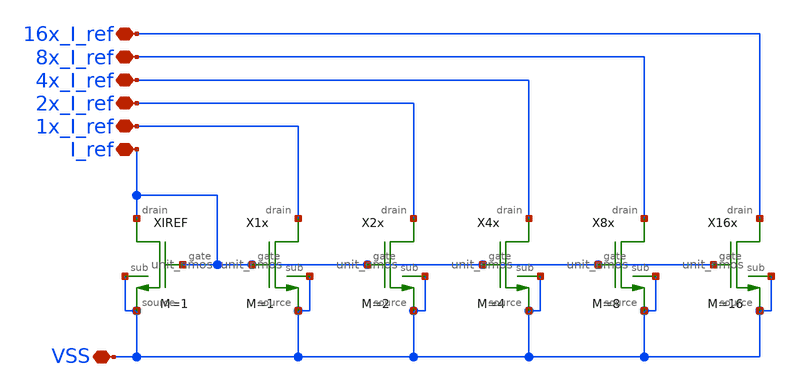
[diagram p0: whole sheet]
** sch_path: designs/libs/core_current_mirror/nmos_current_mirror/nmos_current_mirror.sch
**.subckt nmos_current_mirror I_ref VSS 1x_I_ref 2x_I_ref 4x_I_ref 8x_I_ref 16x_I_ref
*.iopin I_ref
*.iopin VSS
*.iopin 1x_I_ref
*.iopin 2x_I_ref
*.iopin 4x_I_ref
*.iopin 8x_I_ref
*.iopin 16x_I_ref
XIREF I_ref VSS I_ref VSS unit_nmos M=1
X1x 1x_I_ref VSS I_ref VSS unit_nmos M=1
X2x 2x_I_ref VSS I_ref VSS unit_nmos M=2
X4x 4x_I_ref VSS I_ref VSS unit_nmos M=4
X8x 8x_I_ref VSS I_ref VSS unit_nmos M=8
X16x 16x_I_ref VSS I_ref VSS unit_nmos M=16
**.ends

* expanding   symbol:  libs/core_single_mos/unit_nmos/unit_nmos.sym # of pins=4
** sym_path: libs/core_single_mos/unit_nmos/unit_nmos.sym
** sch_path: libs/core_single_mos/unit_nmos/unit_nmos.sch
.subckt unit_nmos drain sub gate source
*.iopin drain
*.iopin source
*.iopin sub
*.iopin gate
XM1 drain gate source sub nfet_03v3 L=0.5u W=12u nf=2 ad='int((nf+1)/2) * W/nf * 0.18u' as='int((nf+2)/2) * W/nf * 0.18u'
+ pd='2*int((nf+1)/2) * (W/nf + 0.18u)' ps='2*int((nf+2)/2) * (W/nf + 0.18u)' nrd='0.18u / W' nrs='0.18u / W'
+ sa=0 sb=0 sd=0 m={M}
**** begin user architecture code

.param M=1

**** end user architecture code
.ends

.end
